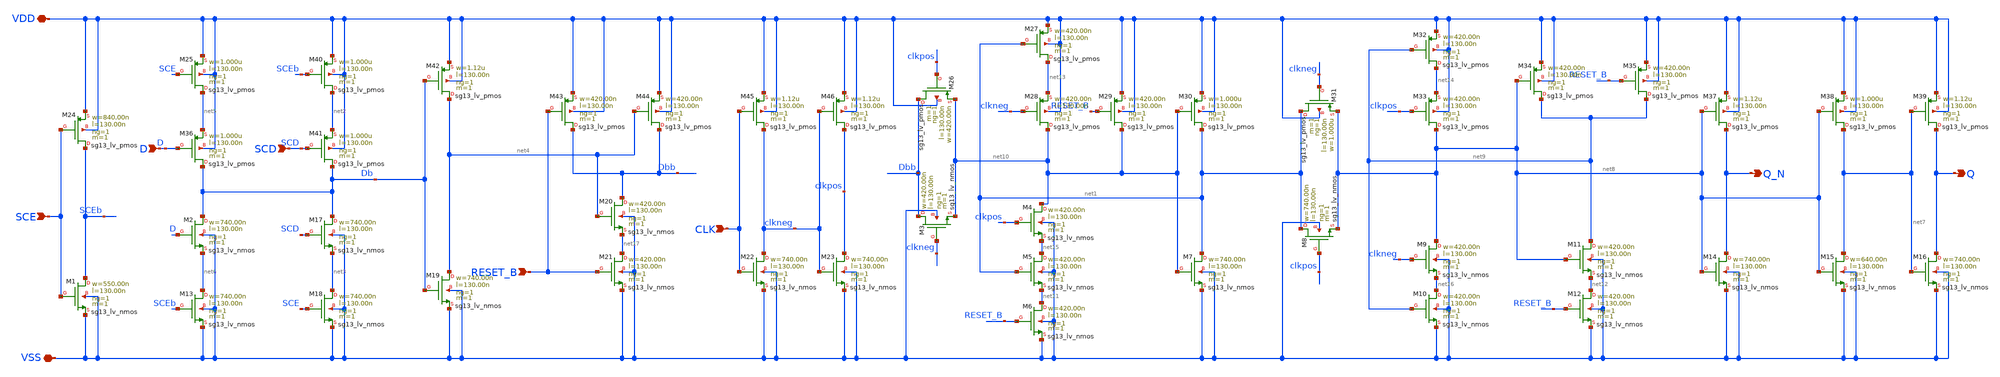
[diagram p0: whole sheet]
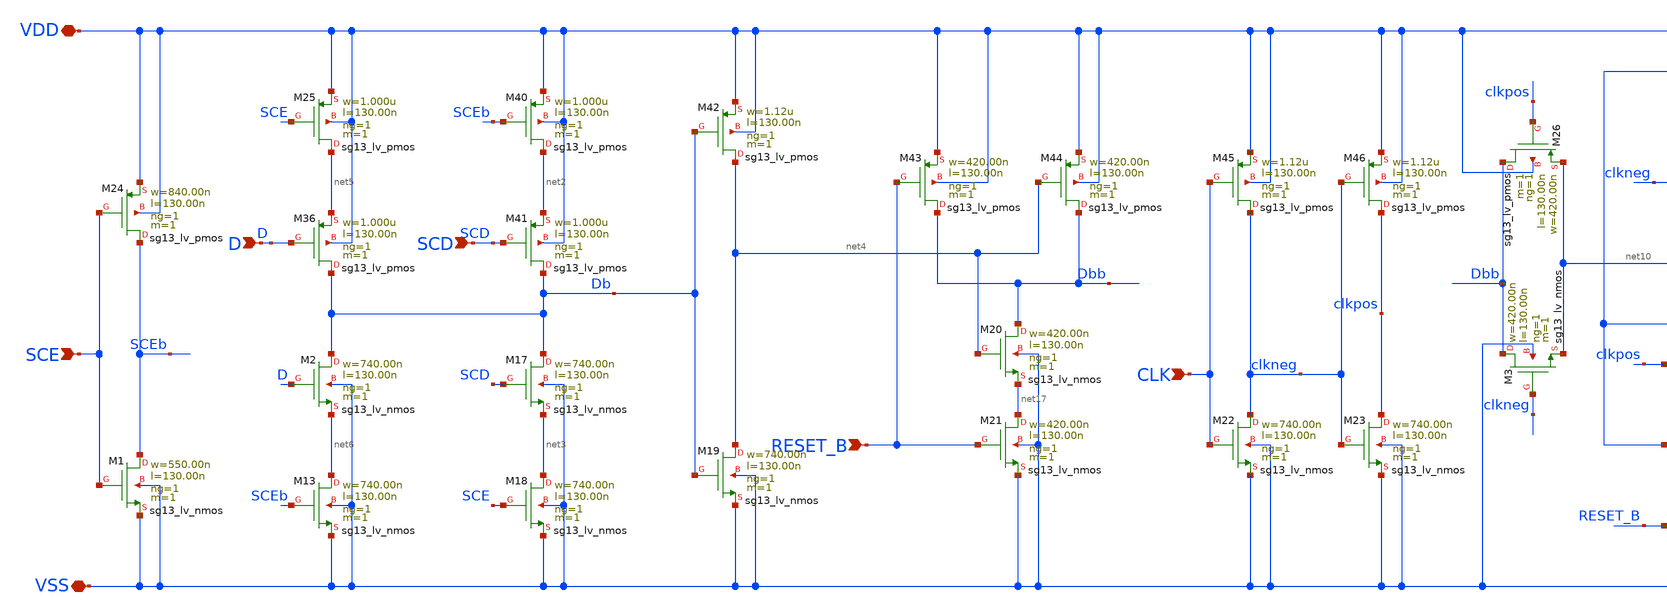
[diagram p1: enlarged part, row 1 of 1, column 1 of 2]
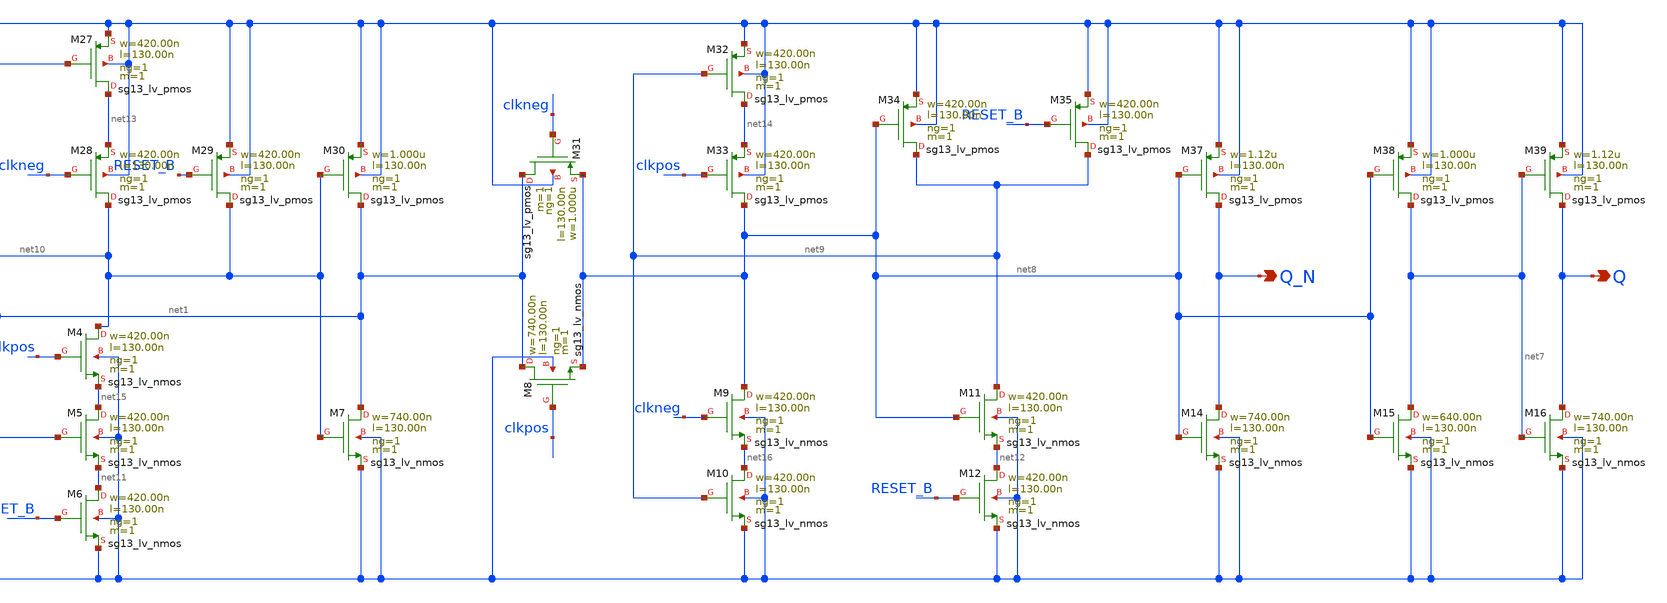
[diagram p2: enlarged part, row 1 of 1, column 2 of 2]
** sch_path: ihp-sg13g2/libs.tech/xschem/sg13g2_stdcells/sg13g2_sdfrbp_1.sch
* Copyright 2023 IHP PDK Authors
* Licensed under the Apache License, Version 2.0 (the "License");
* you may not use this file except in compliance with the License.
* You may obtain a copy of the License at
* https://www.apache.org/licenses/LICENSE-2.0
* Unless required by applicable law or agreed to in writing, software
* distributed under the License is distributed on an "AS IS" BASIS,
* WITHOUT WARRANTIES OR CONDITIONS OF ANY KIND, either express or implied.
* See the License for the specific language governing permissions and
* limitations under the License.
**.subckt sg13g2_sdfrbp_1 Q Q_N CLK D RESET_B SCD SCE VDD VSS
*.opin Q
*.opin Q_N
*.ipin CLK
*.ipin D
*.ipin RESET_B
*.ipin SCD
*.ipin SCE
*.iopin VDD
*.iopin VSS
XM1 SCEb SCE VSS VSS sg13_lv_nmos w=550.00n l=130.00n ng=1 m=1 mm_ok=1
XM2 Db D net6 VSS sg13_lv_nmos w=740.00n l=130.00n ng=1 m=1 mm_ok=1
XM3 Dbb clkneg net10 VSS sg13_lv_nmos w=420.00n l=130.00n ng=1 m=1 mm_ok=1
XM4 net10 clkpos net15 VSS sg13_lv_nmos w=420.00n l=130.00n ng=1 m=1 mm_ok=1
XM5 net15 net1 net11 VSS sg13_lv_nmos w=420.00n l=130.00n ng=1 m=1 mm_ok=1
XM6 net11 RESET_B VSS VSS sg13_lv_nmos w=420.00n l=130.00n ng=1 m=1 mm_ok=1
XM7 net1 net10 VSS VSS sg13_lv_nmos w=740.00n l=130.00n ng=1 m=1 mm_ok=1
XM8 net1 clkpos net8 VSS sg13_lv_nmos w=740.00n l=130.00n ng=1 m=1 mm_ok=1
XM9 net8 clkneg net16 VSS sg13_lv_nmos w=420.00n l=130.00n ng=1 m=1 mm_ok=1
XM10 net16 net9 VSS VSS sg13_lv_nmos w=420.00n l=130.00n ng=1 m=1 mm_ok=1
XM11 net9 net8 net12 VSS sg13_lv_nmos w=420.00n l=130.00n ng=1 m=1 mm_ok=1
XM12 net12 RESET_B VSS VSS sg13_lv_nmos w=420.00n l=130.00n ng=1 m=1 mm_ok=1
XM13 net6 SCEb VSS VSS sg13_lv_nmos w=740.00n l=130.00n ng=1 m=1 mm_ok=1
XM14 Q_N net8 VSS VSS sg13_lv_nmos w=740.00n l=130.00n ng=1 m=1 mm_ok=1
XM15 net7 net8 VSS VSS sg13_lv_nmos w=640.00n l=130.00n ng=1 m=1 mm_ok=1
XM16 Q net7 VSS VSS sg13_lv_nmos w=740.00n l=130.00n ng=1 m=1 mm_ok=1
XM17 Db SCD net3 VSS sg13_lv_nmos w=740.00n l=130.00n ng=1 m=1 mm_ok=1
XM18 net3 SCE VSS VSS sg13_lv_nmos w=740.00n l=130.00n ng=1 m=1 mm_ok=1
XM19 net4 Db VSS VSS sg13_lv_nmos w=740.00n l=130.00n ng=1 m=1 mm_ok=1
XM20 Dbb net4 net17 VSS sg13_lv_nmos w=420.00n l=130.00n ng=1 m=1 mm_ok=1
XM21 net17 RESET_B VSS VSS sg13_lv_nmos w=420.00n l=130.00n ng=1 m=1 mm_ok=1
XM22 clkneg CLK VSS VSS sg13_lv_nmos w=740.00n l=130.00n ng=1 m=1 mm_ok=1
XM23 clkpos clkneg VSS VSS sg13_lv_nmos w=740.00n l=130.00n ng=1 m=1 mm_ok=1
XM24 SCEb SCE VDD VDD sg13_lv_pmos w=840.00n l=130.00n ng=1 m=1 mm_ok=1
XM25 net5 SCE VDD VDD sg13_lv_pmos w=1.000u l=130.00n ng=1 m=1 mm_ok=1
XM26 Dbb clkpos net10 VDD sg13_lv_pmos w=420.00n l=130.00n ng=1 m=1 mm_ok=1
XM27 net13 net1 VDD VDD sg13_lv_pmos w=420.00n l=130.00n ng=1 m=1 mm_ok=1
XM28 net10 clkneg net13 VDD sg13_lv_pmos w=420.00n l=130.00n ng=1 m=1 mm_ok=1
XM29 net10 RESET_B VDD VDD sg13_lv_pmos w=420.00n l=130.00n ng=1 m=1 mm_ok=1
XM30 net1 net10 VDD VDD sg13_lv_pmos w=1.000u l=130.00n ng=1 m=1 mm_ok=1
XM31 net1 clkneg net8 VDD sg13_lv_pmos w=1.000u l=130.00n ng=1 m=1 mm_ok=1
XM32 net14 net9 VDD VDD sg13_lv_pmos w=420.00n l=130.00n ng=1 m=1 mm_ok=1
XM33 net8 clkpos net14 VDD sg13_lv_pmos w=420.00n l=130.00n ng=1 m=1 mm_ok=1
XM34 net9 net8 VDD VDD sg13_lv_pmos w=420.00n l=130.00n ng=1 m=1 mm_ok=1
XM35 net9 RESET_B VDD VDD sg13_lv_pmos w=420.00n l=130.00n ng=1 m=1 mm_ok=1
XM36 Db D net5 VDD sg13_lv_pmos w=1.000u l=130.00n ng=1 m=1 mm_ok=1
XM37 Q_N net8 VDD VDD sg13_lv_pmos w=1.12u l=130.00n ng=1 m=1 mm_ok=1
XM38 net7 net8 VDD VDD sg13_lv_pmos w=1.000u l=130.00n ng=1 m=1 mm_ok=1
XM39 Q net7 VDD VDD sg13_lv_pmos w=1.12u l=130.00n ng=1 m=1 mm_ok=1
XM40 net2 SCEb VDD VDD sg13_lv_pmos w=1.000u l=130.00n ng=1 m=1 mm_ok=1
XM41 Db SCD net2 VDD sg13_lv_pmos w=1.000u l=130.00n ng=1 m=1 mm_ok=1
XM42 net4 Db VDD VDD sg13_lv_pmos w=1.12u l=130.00n ng=1 m=1 mm_ok=1
XM43 Dbb RESET_B VDD VDD sg13_lv_pmos w=420.00n l=130.00n ng=1 m=1 mm_ok=1
XM44 Dbb net4 VDD VDD sg13_lv_pmos w=420.00n l=130.00n ng=1 m=1 mm_ok=1
XM45 clkneg CLK VDD VDD sg13_lv_pmos w=1.12u l=130.00n ng=1 m=1 mm_ok=1
XM46 clkpos clkneg VDD VDD sg13_lv_pmos w=1.12u l=130.00n ng=1 m=1 mm_ok=1
**.ends
.end
